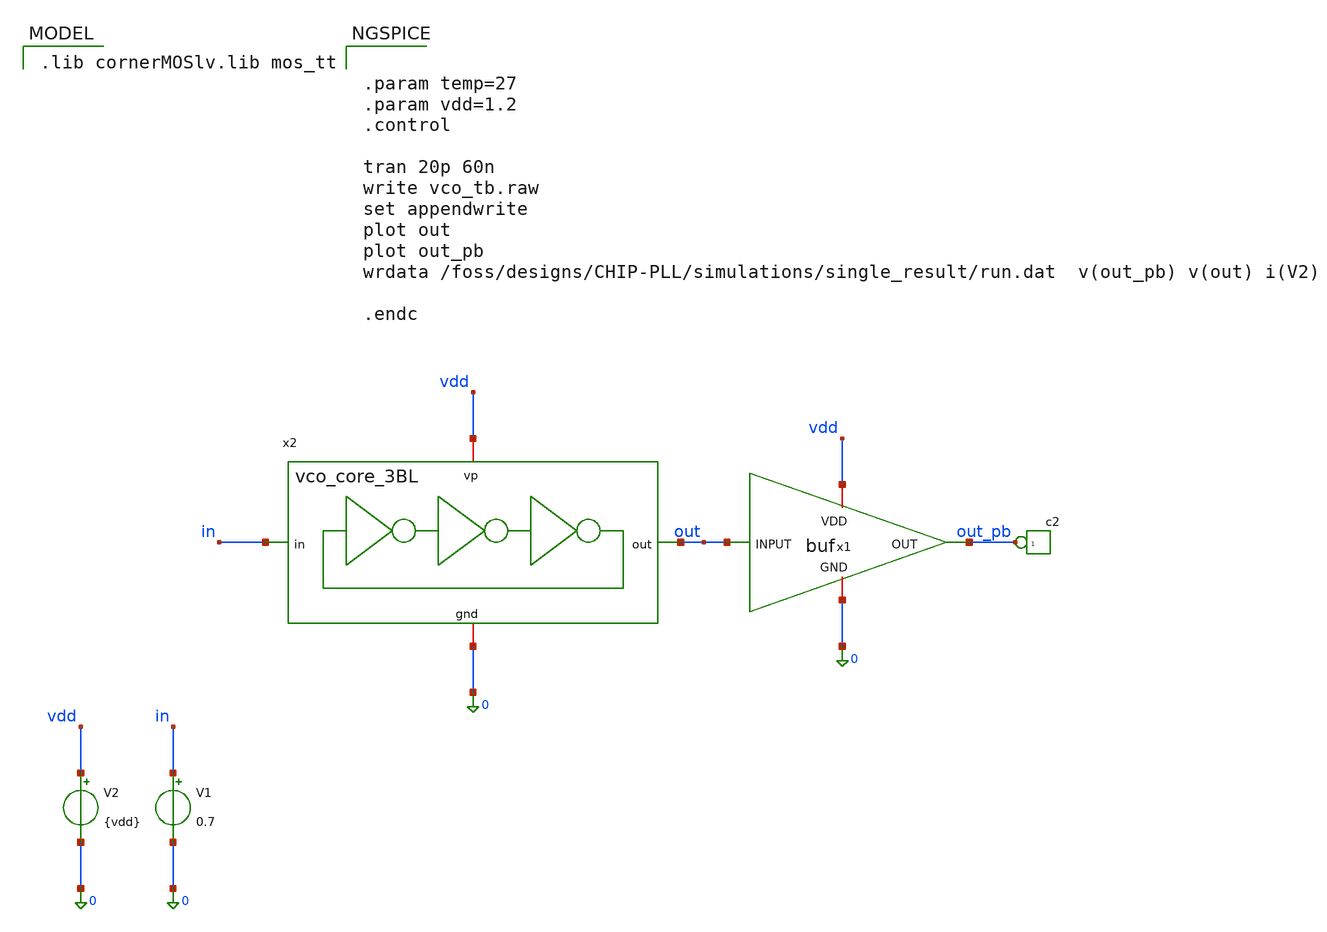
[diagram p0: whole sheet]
** sch_path: vco/vco_tb/vco_dcin_tb_3BL.sch
**.subckt vco_dcin_tb_3BL
V1 in 0 0.7
V2 vdd 0 {vdd}
*connector(1,1) ?1 out_pb
x1 vdd out out_pb 0 buf
x2 vdd 0 out in vco_core_3BL
**** begin user architecture code


.param temp=27
.param vdd=1.2
.control

tran 20p 60n
write vco_tb.raw
set appendwrite
plot out
plot out_pb
wrdata /foss/designs/CHIP-PLL/simulations/single_result/run.dat  v(out_pb) v(out) i(V2)

.endc


 .lib cornerMOSlv.lib mos_tt

**** end user architecture code
**.ends
.end
